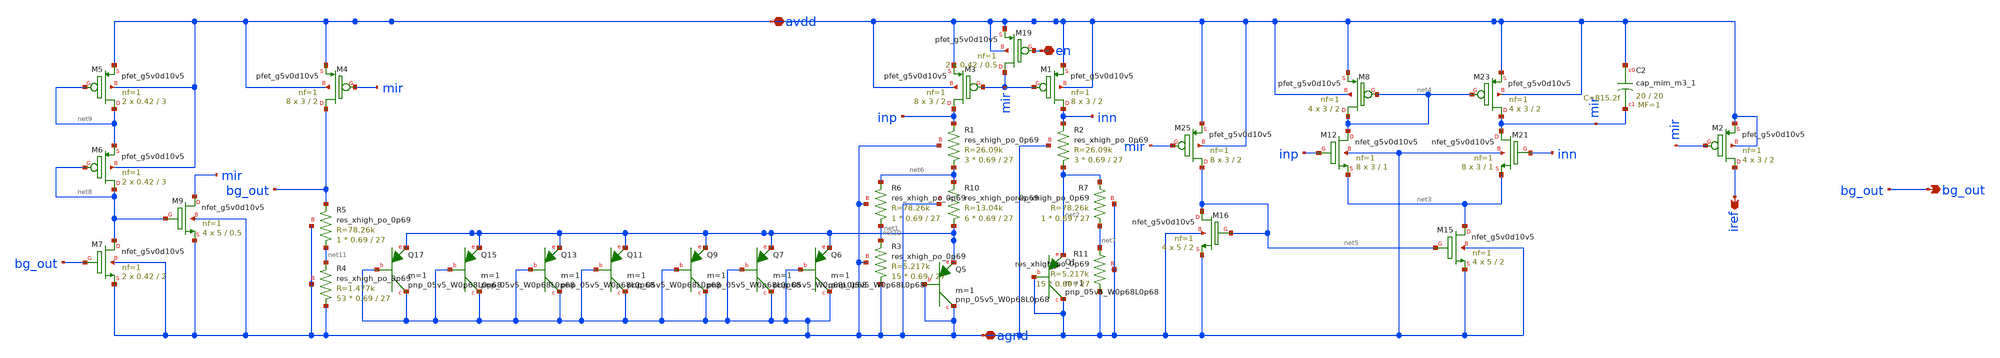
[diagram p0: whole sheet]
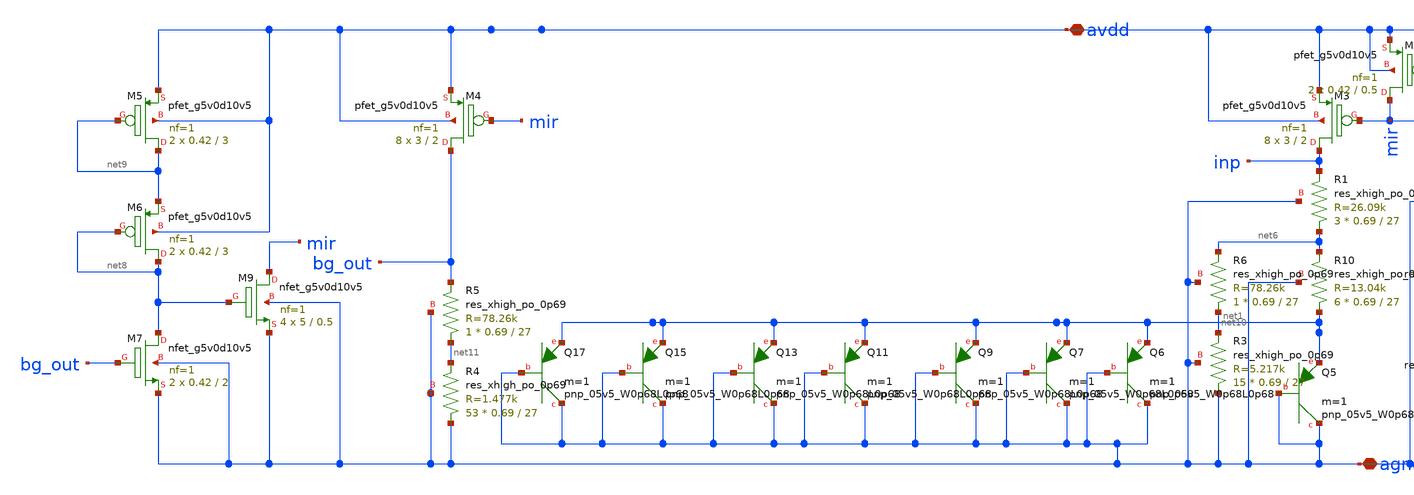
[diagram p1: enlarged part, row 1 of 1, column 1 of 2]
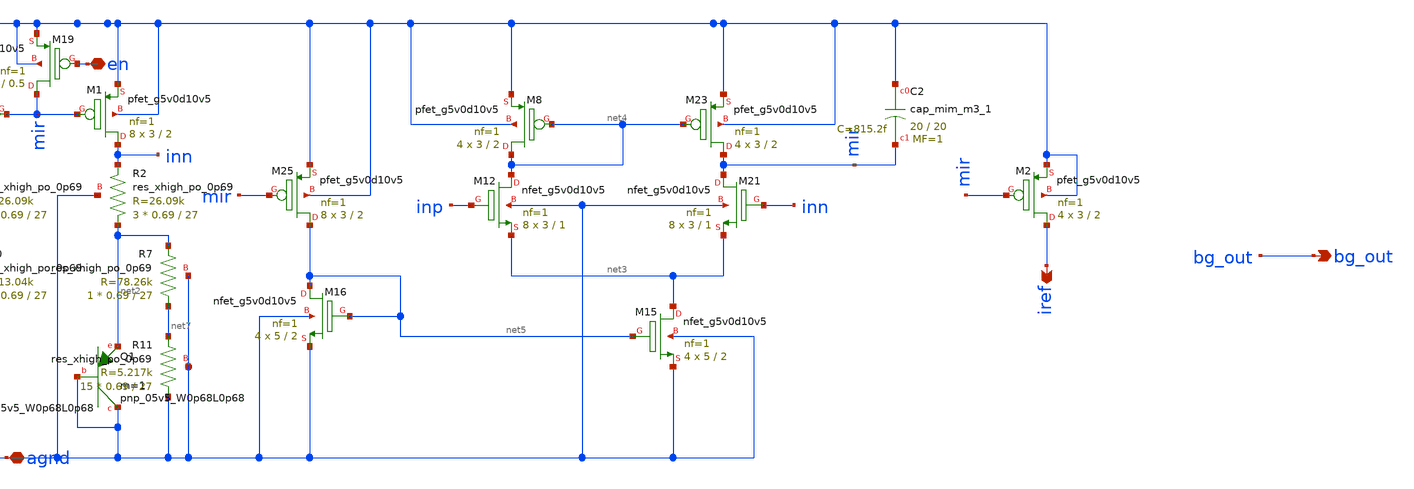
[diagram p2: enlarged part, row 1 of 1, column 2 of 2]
** sch_path: xschem/ldo_v1/bgr_sym.sch
**.subckt bgr_sym avdd agnd bg_out iref en
*.iopin avdd
*.iopin agnd
*.opin bg_out
*.opin iref
*.iopin en
XM2 iref mir avdd avdd sky130_fd_pr__pfet_g5v0d10v5 L=2 W=3 nf=1 ad='int((nf+1)/2) * W/nf * 0.29' as='int((nf+2)/2) * W/nf * 0.29'
+ pd='2*int((nf+1)/2) * (W/nf + 0.29)' ps='2*int((nf+2)/2) * (W/nf + 0.29)' nrd='0.29 / W' nrs='0.29 / W'
+ sa=0 sb=0 sd=0 mult=4 m=4
XM1 inn mir avdd avdd sky130_fd_pr__pfet_g5v0d10v5 L=2 W=3 nf=1 ad='int((nf+1)/2) * W/nf * 0.29' as='int((nf+2)/2) * W/nf * 0.29'
+ pd='2*int((nf+1)/2) * (W/nf + 0.29)' ps='2*int((nf+2)/2) * (W/nf + 0.29)' nrd='0.29 / W' nrs='0.29 / W'
+ sa=0 sb=0 sd=0 mult=8 m=8
XM3 inp mir avdd avdd sky130_fd_pr__pfet_g5v0d10v5 L=2 W=3 nf=1 ad='int((nf+1)/2) * W/nf * 0.29' as='int((nf+2)/2) * W/nf * 0.29'
+ pd='2*int((nf+1)/2) * (W/nf + 0.29)' ps='2*int((nf+2)/2) * (W/nf + 0.29)' nrd='0.29 / W' nrs='0.29 / W'
+ sa=0 sb=0 sd=0 mult=8 m=8
XM4 bg_out mir avdd avdd sky130_fd_pr__pfet_g5v0d10v5 L=2 W=3 nf=1 ad='int((nf+1)/2) * W/nf * 0.29' as='int((nf+2)/2) * W/nf * 0.29'
+ pd='2*int((nf+1)/2) * (W/nf + 0.29)' ps='2*int((nf+2)/2) * (W/nf + 0.29)' nrd='0.29 / W' nrs='0.29 / W'
+ sa=0 sb=0 sd=0 mult=8 m=8
XQ1 agnd agnd net2 sky130_fd_pr__pnp_05v5_W0p68L0p68 m=1
XQ5 agnd agnd net1 sky130_fd_pr__pnp_05v5_W0p68L0p68 m=1
XQ6 agnd agnd net1 sky130_fd_pr__pnp_05v5_W0p68L0p68 m=1
XQ7 agnd agnd net1 sky130_fd_pr__pnp_05v5_W0p68L0p68 m=1
XQ9 agnd agnd net1 sky130_fd_pr__pnp_05v5_W0p68L0p68 m=1
XQ11 agnd agnd net1 sky130_fd_pr__pnp_05v5_W0p68L0p68 m=1
XQ13 agnd agnd net1 sky130_fd_pr__pnp_05v5_W0p68L0p68 m=1
XQ15 agnd agnd net1 sky130_fd_pr__pnp_05v5_W0p68L0p68 m=1
XQ17 agnd agnd net1 sky130_fd_pr__pnp_05v5_W0p68L0p68 m=1
XM8 net4 net4 avdd avdd sky130_fd_pr__pfet_g5v0d10v5 L=2 W=3 nf=1 ad='int((nf+1)/2) * W/nf * 0.29' as='int((nf+2)/2) * W/nf * 0.29'
+ pd='2*int((nf+1)/2) * (W/nf + 0.29)' ps='2*int((nf+2)/2) * (W/nf + 0.29)' nrd='0.29 / W' nrs='0.29 / W'
+ sa=0 sb=0 sd=0 mult=4 m=4
XM12 net4 inp net3 agnd sky130_fd_pr__nfet_g5v0d10v5 L=1 W=3 nf=1 ad='int((nf+1)/2) * W/nf * 0.29' as='int((nf+2)/2) * W/nf * 0.29'
+ pd='2*int((nf+1)/2) * (W/nf + 0.29)' ps='2*int((nf+2)/2) * (W/nf + 0.29)' nrd='0.29 / W' nrs='0.29 / W'
+ sa=0 sb=0 sd=0 mult=8 m=8
XM21 mir inn net3 agnd sky130_fd_pr__nfet_g5v0d10v5 L=1 W=3 nf=1 ad='int((nf+1)/2) * W/nf * 0.29' as='int((nf+2)/2) * W/nf * 0.29'
+ pd='2*int((nf+1)/2) * (W/nf + 0.29)' ps='2*int((nf+2)/2) * (W/nf + 0.29)' nrd='0.29 / W' nrs='0.29 / W'
+ sa=0 sb=0 sd=0 mult=8 m=8
XM23 mir net4 avdd avdd sky130_fd_pr__pfet_g5v0d10v5 L=2 W=3 nf=1 ad='int((nf+1)/2) * W/nf * 0.29' as='int((nf+2)/2) * W/nf * 0.29'
+ pd='2*int((nf+1)/2) * (W/nf + 0.29)' ps='2*int((nf+2)/2) * (W/nf + 0.29)' nrd='0.29 / W' nrs='0.29 / W'
+ sa=0 sb=0 sd=0 mult=4 m=4
XM15 net3 net5 agnd agnd sky130_fd_pr__nfet_g5v0d10v5 L=2 W=5 nf=1 ad='int((nf+1)/2) * W/nf * 0.29' as='int((nf+2)/2) * W/nf * 0.29'
+ pd='2*int((nf+1)/2) * (W/nf + 0.29)' ps='2*int((nf+2)/2) * (W/nf + 0.29)' nrd='0.29 / W' nrs='0.29 / W'
+ sa=0 sb=0 sd=0 mult=4 m=4
XM25 net5 mir avdd avdd sky130_fd_pr__pfet_g5v0d10v5 L=2 W=3 nf=1 ad='int((nf+1)/2) * W/nf * 0.29' as='int((nf+2)/2) * W/nf * 0.29'
+ pd='2*int((nf+1)/2) * (W/nf + 0.29)' ps='2*int((nf+2)/2) * (W/nf + 0.29)' nrd='0.29 / W' nrs='0.29 / W'
+ sa=0 sb=0 sd=0 mult=8 m=8
XM16 net5 net5 agnd agnd sky130_fd_pr__nfet_g5v0d10v5 L=2 W=5 nf=1 ad='int((nf+1)/2) * W/nf * 0.29' as='int((nf+2)/2) * W/nf * 0.29'
+ pd='2*int((nf+1)/2) * (W/nf + 0.29)' ps='2*int((nf+2)/2) * (W/nf + 0.29)' nrd='0.29 / W' nrs='0.29 / W'
+ sa=0 sb=0 sd=0 mult=4 m=4
XR1 net6 inp agnd sky130_fd_pr__res_xhigh_po_0p69 L=27 mult=3 m=3
XR2 net2 inn agnd sky130_fd_pr__res_xhigh_po_0p69 L=27 mult=3 m=3
XR10 net1 net6 agnd sky130_fd_pr__res_xhigh_po_0p69 L=27 mult=6 m=6
XR11 agnd net7 agnd sky130_fd_pr__res_xhigh_po_0p69 L=27 mult=15 m=15
XR6 net10 net6 agnd sky130_fd_pr__res_xhigh_po_0p69 L=27 mult=1 m=1
XR5 net11 bg_out agnd sky130_fd_pr__res_xhigh_po_0p69 L=27 mult=1 m=1
XM19 mir en avdd avdd sky130_fd_pr__pfet_g5v0d10v5 L=0.5 W=0.42 nf=1 ad='int((nf+1)/2) * W/nf * 0.29'
+ as='int((nf+2)/2) * W/nf * 0.29' pd='2*int((nf+1)/2) * (W/nf + 0.29)' ps='2*int((nf+2)/2) * (W/nf + 0.29)'
+ nrd='0.29 / W' nrs='0.29 / W' sa=0 sb=0 sd=0 mult=2 m=2
XC2 avdd mir sky130_fd_pr__cap_mim_m3_1 W=20 L=20 MF=1 m=1
XM5 net9 net9 avdd avdd sky130_fd_pr__pfet_g5v0d10v5 L=3 W=0.42 nf=1 ad='int((nf+1)/2) * W/nf * 0.29'
+ as='int((nf+2)/2) * W/nf * 0.29' pd='2*int((nf+1)/2) * (W/nf + 0.29)' ps='2*int((nf+2)/2) * (W/nf + 0.29)'
+ nrd='0.29 / W' nrs='0.29 / W' sa=0 sb=0 sd=0 mult=2 m=2
XM6 net8 net8 net9 avdd sky130_fd_pr__pfet_g5v0d10v5 L=3 W=0.42 nf=1 ad='int((nf+1)/2) * W/nf * 0.29'
+ as='int((nf+2)/2) * W/nf * 0.29' pd='2*int((nf+1)/2) * (W/nf + 0.29)' ps='2*int((nf+2)/2) * (W/nf + 0.29)'
+ nrd='0.29 / W' nrs='0.29 / W' sa=0 sb=0 sd=0 mult=2 m=2
XM7 net8 bg_out agnd agnd sky130_fd_pr__nfet_g5v0d10v5 L=2 W=0.42 nf=1 ad='int((nf+1)/2) * W/nf * 0.29'
+ as='int((nf+2)/2) * W/nf * 0.29' pd='2*int((nf+1)/2) * (W/nf + 0.29)' ps='2*int((nf+2)/2) * (W/nf + 0.29)'
+ nrd='0.29 / W' nrs='0.29 / W' sa=0 sb=0 sd=0 mult=2 m=2
XM9 mir net8 agnd agnd sky130_fd_pr__nfet_g5v0d10v5 L=0.5 W=5 nf=1 ad='int((nf+1)/2) * W/nf * 0.29' as='int((nf+2)/2) * W/nf * 0.29'
+ pd='2*int((nf+1)/2) * (W/nf + 0.29)' ps='2*int((nf+2)/2) * (W/nf + 0.29)' nrd='0.29 / W' nrs='0.29 / W'
+ sa=0 sb=0 sd=0 mult=4 m=4
XR3 agnd net10 agnd sky130_fd_pr__res_xhigh_po_0p69 L=27 mult=15 m=15
XR4 agnd net11 agnd sky130_fd_pr__res_xhigh_po_0p69 L=27 mult=53 m=53
XR7 net7 net2 agnd sky130_fd_pr__res_xhigh_po_0p69 L=27 mult=1 m=1
**.ends
.end
